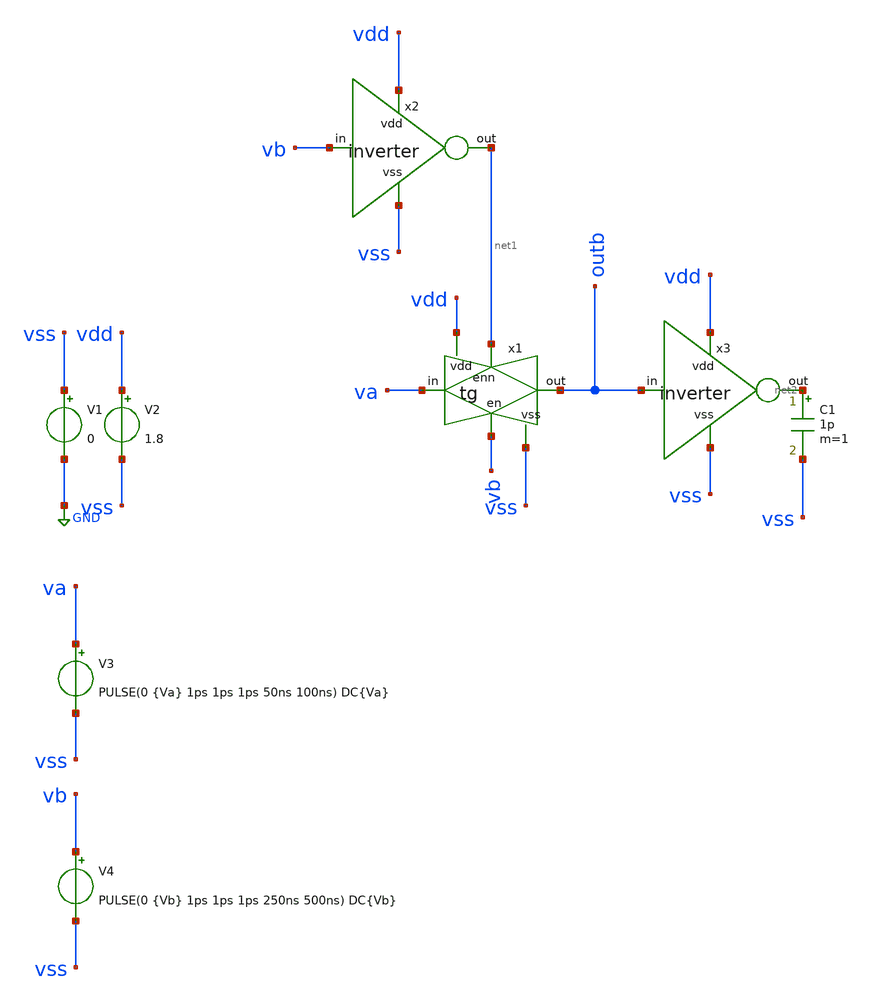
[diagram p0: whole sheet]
** sch_path: track_vlsi/ledesma/sch/tb_tg.sch
**.subckt tb_tg
V1 vss GND 0
V2 vdd vss 1.8
V3 va vss PULSE(0 {Va} 1ps 1ps 1ps 50ns 100ns) DC{Va}
V4 vb vss PULSE(0 {Vb} 1ps 1ps 1ps 250ns 500ns) DC{Vb}
x3 vdd net2 outb vss inverter
C1 net2 vss 1p m=1
x1 vdd net1 outb va vb vss tg
x2 vdd net1 vb vss inverter
**** begin user architecture code



* Parametros del circuito
.param Va=1.8
.param Vb=1.8
.options TEMP = 27.0

* Include
.lib /home/eamta/skywater/skywater-pdk/libraries/sky130_fd_pr_ngspice/latest/models/corners/sky130.lib TT

*simulation
.control
  tran 10ps 500ns
  setplot tran1
  plot v(outb) v(Va) V(Vb)
  write tb_and_tran.raw

  reset
  dc V3 0 1.8 0.01
  setplot dc1
  plot v(outb) v(Va)
  write tb_inverter_dc.raw


.endc
.end


**** end user architecture code
**.ends
.GLOBAL GND
.end
